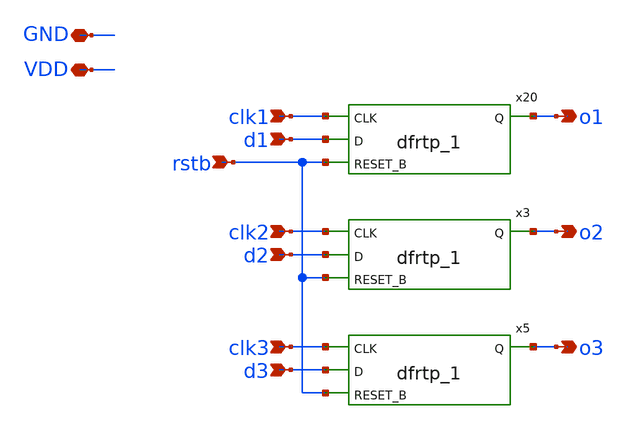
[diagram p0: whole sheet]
** sch_path: xschem/readout/counter_ro.sch
**.subckt counter_ro VDD GND rstb clk1 d1 clk2 clk3 d2 d3 o1 o2 o3
*.iopin VDD
*.iopin GND
*.ipin rstb
*.ipin clk1
*.ipin d1
*.ipin clk2
*.ipin clk3
*.ipin d2
*.ipin d3
*.opin o1
*.opin o2
*.opin o3
x20 clk1 d1 rstb GND GND VDD VDD o1 sky130_fd_sc_lp__dfrtp_1
x3 clk2 d2 rstb GND GND VDD VDD o2 sky130_fd_sc_lp__dfrtp_1
x5 clk3 d3 rstb GND GND VDD VDD o3 sky130_fd_sc_lp__dfrtp_1
**.ends
.end
